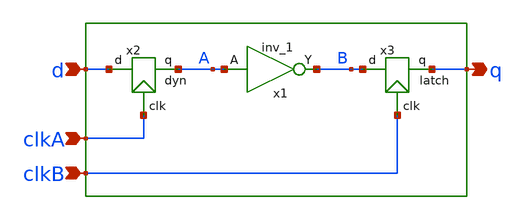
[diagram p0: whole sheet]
** sch_path: src/xe/test_cases/dyn_latch.sch
**.subckt dyn_latch d clkA q clkB
*.ipin d
*.ipin clkA
*.opin q
*.ipin clkB
x1 A vcc vcc vss vss B sky130_fd_sc_hd__inv_1
x3 clkB q B latch
x2 clkA A d dyn vcc=vss vss=vss
**.ends

* expanding   symbol:  yxt/latch.sym # of pins=3
** sym_path: src/xe/test_cases/latch.sym
** sch_path: src/xe/test_cases/latch.sch
.subckt latch clk q d  vcc=vcc vss=vss
*.ipin clk
*.ipin d
*.opin q
x1 d vcc vcc vss vss db sky130_fd_sc_hd__inv_1
x2 clkb db z clk tgate vcc=vcc vss=vss
x3 z vcc vcc vss vss q sky130_fd_sc_hd__inv_1
x6 clk vcc vcc vss vss clkb sky130_fd_sc_hd__inv_1
x4 z vcc vcc vss vss fb sky130_fd_sc_hd__inv_1
x5 fb vcc vcc vss vss z sky130_fd_sc_hd__inv_1
.ends


* expanding   symbol:  yxt/dyn.sym # of pins=3
** sym_path: src/xe/test_cases/dyn.sym
** sch_path: src/xe/test_cases/dyn.sch
.subckt dyn clk q d  vcc=vss vss=vss
*.ipin clk
*.opin q
*.ipin d
x1 net1 vcc vcc vss vss q sky130_fd_sc_hd__inv_1
XM1 net1 d net2 net3 sky130_fd_pr__nfet_01v8 L=0.15 W=1 nf=1 ad='int((nf+1)/2) * W/nf * 0.29' as='int((nf+2)/2) * W/nf * 0.29'
+ pd='2*int((nf+1)/2) * (W/nf + 0.29)' ps='2*int((nf+2)/2) * (W/nf + 0.29)' nrd='0.29 / W' nrs='0.29 / W'
+ sa=0 sb=0 sd=0 mult=1 m=1
XM2 net1 q vcc net4 sky130_fd_pr__pfet_01v8 L=0.15 W=1 nf=1 ad='int((nf+1)/2) * W/nf * 0.29' as='int((nf+2)/2) * W/nf * 0.29'
+ pd='2*int((nf+1)/2) * (W/nf + 0.29)' ps='2*int((nf+2)/2) * (W/nf + 0.29)' nrd='0.29 / W' nrs='0.29 / W'
+ sa=0 sb=0 sd=0 mult=1 m=1
XM3 net1 clk vcc net5 sky130_fd_pr__pfet_01v8 L=0.15 W=1 nf=1 ad='int((nf+1)/2) * W/nf * 0.29' as='int((nf+2)/2) * W/nf * 0.29'
+ pd='2*int((nf+1)/2) * (W/nf + 0.29)' ps='2*int((nf+2)/2) * (W/nf + 0.29)' nrd='0.29 / W' nrs='0.29 / W'
+ sa=0 sb=0 sd=0 mult=1 m=1
XM4 net2 clk vss net6 sky130_fd_pr__nfet_01v8 L=0.15 W=1 nf=1 ad='int((nf+1)/2) * W/nf * 0.29' as='int((nf+2)/2) * W/nf * 0.29'
+ pd='2*int((nf+1)/2) * (W/nf + 0.29)' ps='2*int((nf+2)/2) * (W/nf + 0.29)' nrd='0.29 / W' nrs='0.29 / W'
+ sa=0 sb=0 sd=0 mult=1 m=1
.ends


* expanding   symbol:  yxt/tgate.sym # of pins=4
** sym_path: src/xe/test_cases/tgate.sym
** sch_path: src/xe/test_cases/tgate.sch
.subckt tgate gp s d gn  vcc=vcc vss=vss
*.ipin s
*.ipin gp
*.ipin gn
*.opin d
XMpc d gp s vss sky130_fd_pr__pfet_01v8 L=0.15 W=1 nf=1 ad='int((nf+1)/2) * W/nf * 0.29' as='int((nf+2)/2) * W/nf * 0.29'
+ pd='2*int((nf+1)/2) * (W/nf + 0.29)' ps='2*int((nf+2)/2) * (W/nf + 0.29)' nrd='0.29 / W' nrs='0.29 / W'
+ sa=0 sb=0 sd=0 mult=7 m=7
XM15 s gn d vcc sky130_fd_pr__nfet_01v8 L=0.15 W=1 nf=1 ad='int((nf+1)/2) * W/nf * 0.29' as='int((nf+2)/2) * W/nf * 0.29'
+ pd='2*int((nf+1)/2) * (W/nf + 0.29)' ps='2*int((nf+2)/2) * (W/nf + 0.29)' nrd='0.29 / W' nrs='0.29 / W'
+ sa=0 sb=0 sd=0 mult=1 m=1
.ends

.end
